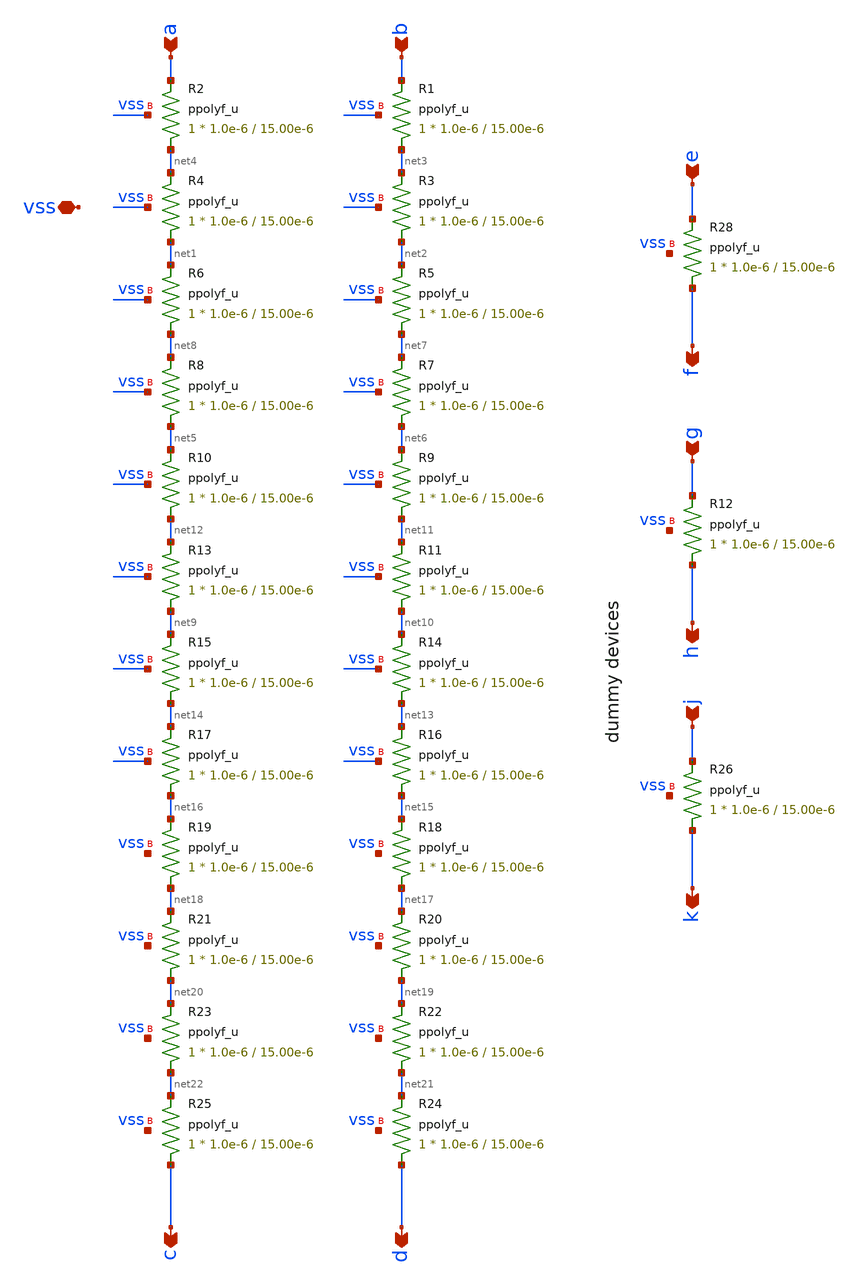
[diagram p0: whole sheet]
** sch_path: projects/programmable_transceiver_platform/analog/core_support/bandgap/xschem/bg_res.sch
**.subckt bg_res a b c d vss f e h g k j
*.ipin a
*.ipin b
*.opin c
*.opin d
*.iopin vss
*.opin f
*.ipin e
*.opin h
*.ipin g
*.opin k
*.ipin j
XR28 f e vss ppolyf_u r_width=1.0e-6 r_length=15.00e-6 m=1
XR12 h g vss ppolyf_u r_width=1.0e-6 r_length=15.00e-6 m=1
XR1 net3 b vss ppolyf_u r_width=1.0e-6 r_length=15.00e-6 m=1
XR2 net4 a vss ppolyf_u r_width=1.0e-6 r_length=15.00e-6 m=1
XR3 net2 net3 vss ppolyf_u r_width=1.0e-6 r_length=15.00e-6 m=1
XR4 net1 net4 vss ppolyf_u r_width=1.0e-6 r_length=15.00e-6 m=1
XR5 net7 net2 vss ppolyf_u r_width=1.0e-6 r_length=15.00e-6 m=1
XR6 net8 net1 vss ppolyf_u r_width=1.0e-6 r_length=15.00e-6 m=1
XR7 net6 net7 vss ppolyf_u r_width=1.0e-6 r_length=15.00e-6 m=1
XR8 net5 net8 vss ppolyf_u r_width=1.0e-6 r_length=15.00e-6 m=1
XR9 net11 net6 vss ppolyf_u r_width=1.0e-6 r_length=15.00e-6 m=1
XR10 net12 net5 vss ppolyf_u r_width=1.0e-6 r_length=15.00e-6 m=1
XR11 net10 net11 vss ppolyf_u r_width=1.0e-6 r_length=15.00e-6 m=1
XR13 net9 net12 vss ppolyf_u r_width=1.0e-6 r_length=15.00e-6 m=1
XR14 net13 net10 vss ppolyf_u r_width=1.0e-6 r_length=15.00e-6 m=1
XR15 net14 net9 vss ppolyf_u r_width=1.0e-6 r_length=15.00e-6 m=1
XR16 net15 net13 vss ppolyf_u r_width=1.0e-6 r_length=15.00e-6 m=1
XR17 net16 net14 vss ppolyf_u r_width=1.0e-6 r_length=15.00e-6 m=1
XR18 net17 net15 vss ppolyf_u r_width=1.0e-6 r_length=15.00e-6 m=1
XR19 net18 net16 vss ppolyf_u r_width=1.0e-6 r_length=15.00e-6 m=1
XR20 net19 net17 vss ppolyf_u r_width=1.0e-6 r_length=15.00e-6 m=1
XR21 net20 net18 vss ppolyf_u r_width=1.0e-6 r_length=15.00e-6 m=1
XR22 net21 net19 vss ppolyf_u r_width=1.0e-6 r_length=15.00e-6 m=1
XR23 net22 net20 vss ppolyf_u r_width=1.0e-6 r_length=15.00e-6 m=1
XR24 d net21 vss ppolyf_u r_width=1.0e-6 r_length=15.00e-6 m=1
XR25 c net22 vss ppolyf_u r_width=1.0e-6 r_length=15.00e-6 m=1
XR26 k j vss ppolyf_u r_width=1.0e-6 r_length=15.00e-6 m=1
**.ends
.end
